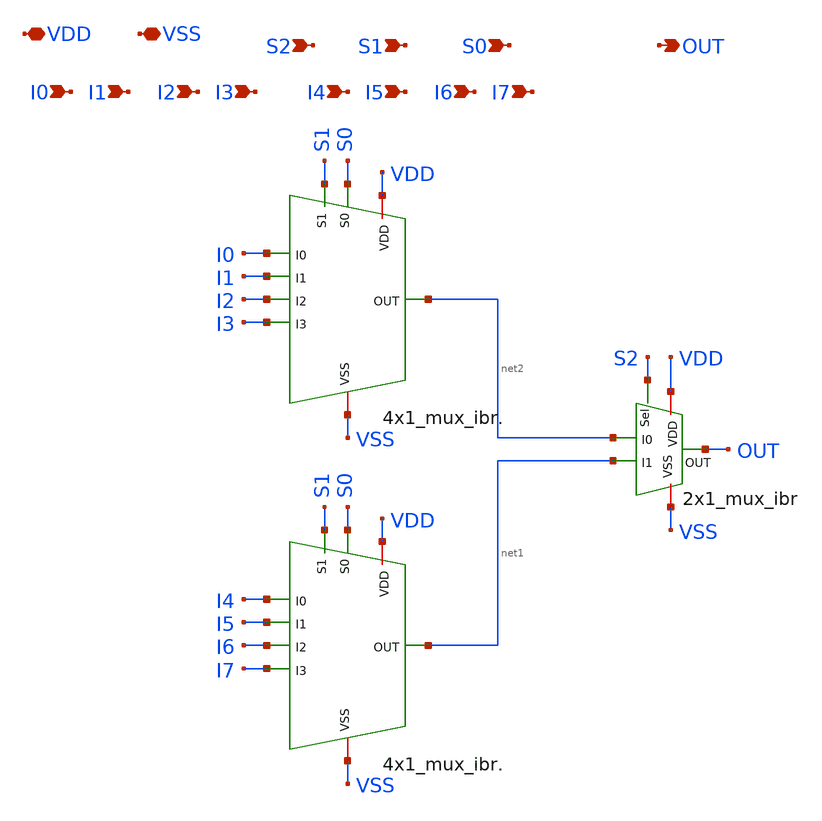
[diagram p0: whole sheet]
** sch_path: Clock_Generator_PAKISTAN_02/Schematics/8x1_mux_ibr..sch
**.subckt 8x1_mux_ibr. VDD VSS S1 OUT S0 I6 I7 I4 I5 I2 I3 I0 I1 S2
*.iopin VDD
*.iopin VSS
*.ipin S1
*.opin OUT
*.ipin S0
*.ipin I6
*.ipin I7
*.ipin I4
*.ipin I5
*.ipin I2
*.ipin I3
*.ipin I0
*.ipin I1
*.ipin S2
x2 VDD S1 VSS I2 I3 S0 I0 I1 net2 4x1_mux_ibr.
x3 VDD S1 VSS I6 I7 S0 I4 I5 net1 4x1_mux_ibr.
x1 VSS S2 OUT net2 net1 VDD 2x1_mux_ibr
**.ends
.end
